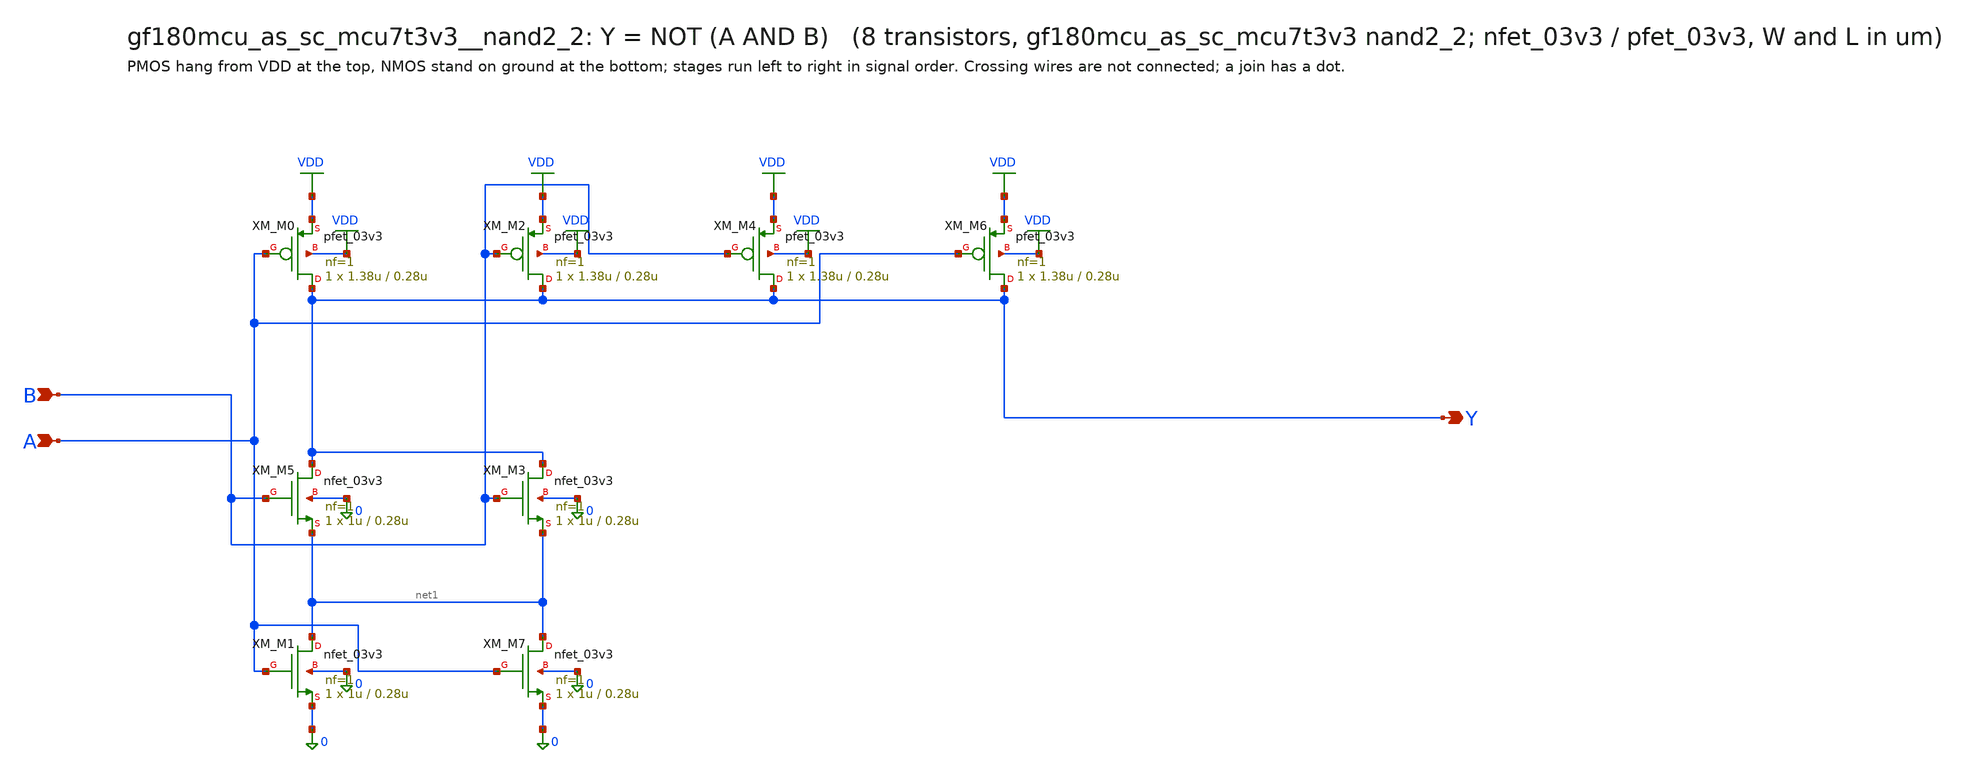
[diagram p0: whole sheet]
** sch_path: xschem/cells_tx/gf180mcu_as_sc_mcu7t3v3__nand2_2.sch
**.subckt gf180mcu_as_sc_mcu7t3v3__nand2_2 B A Y
*.ipin B
*.ipin A
*.opin Y
XM_M0 Y A VDD VDD pfet_03v3 L=0.28u W=1.38u nf=1 ad=3.588e-13 as=3.588e-13 pd=1.9e-06 ps=1.9e-06
+ nrd=0 nrs=0 sa=0 sb=0 sd=0 m=1
XM_M1 net1 A 0 0 nfet_03v3 L=0.28u W=1u nf=1 ad=2.6e-13 as=4.4e-13 pd=1.52e-06 ps=2.88e-06 nrd=0
+ nrs=0 sa=0 sb=0 sd=0 m=1
XM_M2 Y B VDD VDD pfet_03v3 L=0.28u W=1.38u nf=1 ad=3.588e-13 as=3.588e-13 pd=1.9e-06 ps=1.9e-06
+ nrd=0 nrs=0 sa=0 sb=0 sd=0 m=1
XM_M3 Y B net1 0 nfet_03v3 L=0.28u W=1u nf=1 ad=5.15e-13 as=2.6e-13 pd=3.03e-06 ps=1.52e-06 nrd=0
+ nrs=0 sa=0 sb=0 sd=0 m=1
XM_M4 Y B VDD VDD pfet_03v3 L=0.28u W=1.38u nf=1 ad=7.176e-13 as=3.588e-13 pd=3.8e-06 ps=1.9e-06
+ nrd=0 nrs=0 sa=0 sb=0 sd=0 m=1
XM_M5 Y B net1 0 nfet_03v3 L=0.28u W=1u nf=1 ad=2.6e-13 as=2.6e-13 pd=1.52e-06 ps=1.52e-06 nrd=0
+ nrs=0 sa=0 sb=0 sd=0 m=1
XM_M6 Y A VDD VDD pfet_03v3 L=0.28u W=1.38u nf=1 ad=3.588e-13 as=6.072e-13 pd=1.9e-06 ps=3.64e-06
+ nrd=0 nrs=0 sa=0 sb=0 sd=0 m=1
XM_M7 net1 A 0 0 nfet_03v3 L=0.28u W=1u nf=1 ad=2.6e-13 as=2.6e-13 pd=1.52e-06 ps=1.52e-06 nrd=0
+ nrs=0 sa=0 sb=0 sd=0 m=1
**.ends
.GLOBAL VDD
.end
